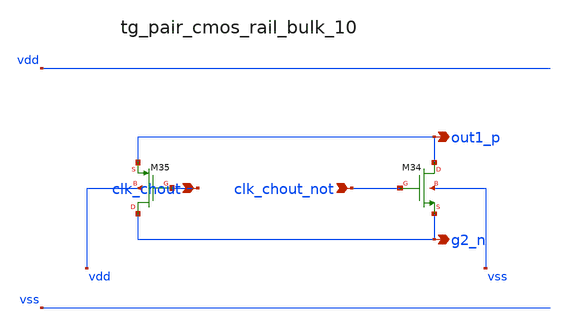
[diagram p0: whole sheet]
** sch_path: analog-db/raw/ia_003_fan_chopper_pf/hier/blocks/tg_pair_cmos_rail_bulk_10.sch
**.subckt tg_pair_cmos_rail_bulk_10 clk_chout clk_chout_not out1_p g2_n
*.ipin clk_chout
*.ipin clk_chout_not
*.opin out1_p
*.opin g2_n
XM34 out1_p clk_chout_not g2_n vss sg13_lv_nmos w=x_dut_xm34_w l=x_dut_xm34_l ng=1 m=x_dut_xm34_m
XM35 g2_n clk_chout out1_p vdd sg13_lv_pmos w=x_dut_xm35_w l=x_dut_xm35_l ng=1 m=x_dut_xm35_m
**.ends
.end
